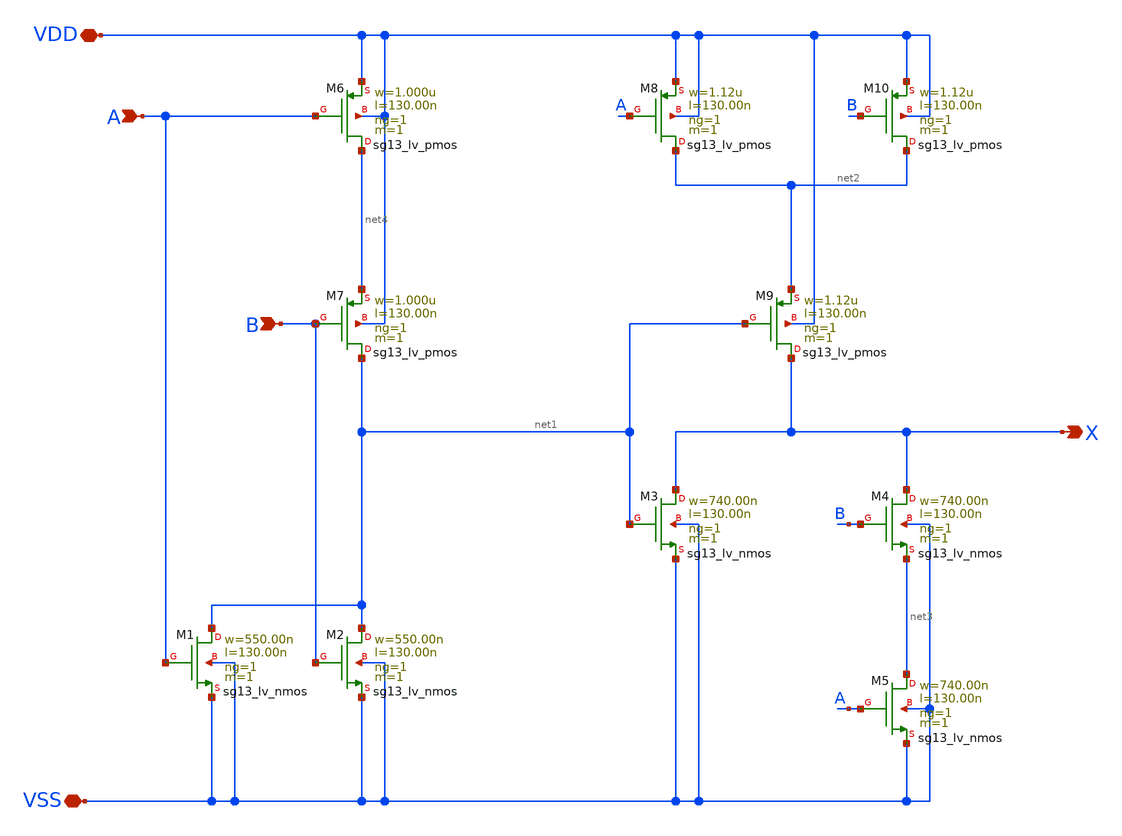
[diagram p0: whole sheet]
** sch_path: ihp-sg13g2/libs.tech/xschem/sg13g2_stdcells/sg13g2_xor2_1.sch
* Copyright 2023 IHP PDK Authors
* Licensed under the Apache License, Version 2.0 (the "License");
* you may not use this file except in compliance with the License.
* You may obtain a copy of the License at
* https://www.apache.org/licenses/LICENSE-2.0
* Unless required by applicable law or agreed to in writing, software
* distributed under the License is distributed on an "AS IS" BASIS,
* WITHOUT WARRANTIES OR CONDITIONS OF ANY KIND, either express or implied.
* See the License for the specific language governing permissions and
* limitations under the License.
**.subckt sg13g2_xor2_1 X B A VDD VSS
*.opin X
*.ipin B
*.ipin A
*.iopin VDD
*.iopin VSS
XM1 net1 A VSS VSS sg13_lv_nmos w=550.00n l=130.00n ng=1 m=1 mm_ok=1
XM2 net1 B VSS VSS sg13_lv_nmos w=550.00n l=130.00n ng=1 m=1 mm_ok=1
XM3 X net1 VSS VSS sg13_lv_nmos w=740.00n l=130.00n ng=1 m=1 mm_ok=1
XM4 X B net3 VSS sg13_lv_nmos w=740.00n l=130.00n ng=1 m=1 mm_ok=1
XM5 net3 A VSS VSS sg13_lv_nmos w=740.00n l=130.00n ng=1 m=1 mm_ok=1
XM6 net4 A VDD VDD sg13_lv_pmos w=1.000u l=130.00n ng=1 m=1 mm_ok=1
XM7 net1 B net4 VDD sg13_lv_pmos w=1.000u l=130.00n ng=1 m=1 mm_ok=1
XM8 net2 A VDD VDD sg13_lv_pmos w=1.12u l=130.00n ng=1 m=1 mm_ok=1
XM9 X net1 net2 VDD sg13_lv_pmos w=1.12u l=130.00n ng=1 m=1 mm_ok=1
XM10 net2 B VDD VDD sg13_lv_pmos w=1.12u l=130.00n ng=1 m=1 mm_ok=1
**.ends
.end
